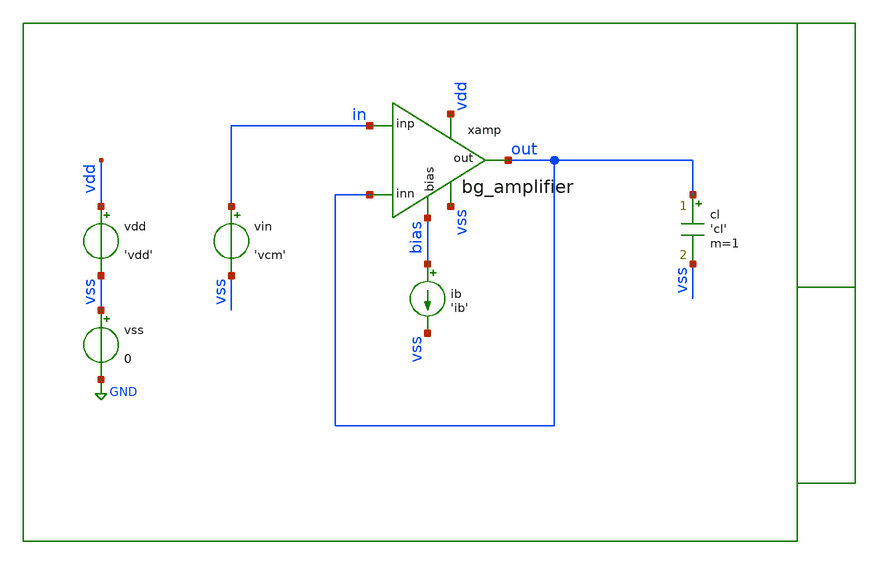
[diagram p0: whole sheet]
** sch_path: xschem/tb/bandgap_cm/bg_amplifier/dc_bg_amplifier_icmr.sch
**.subckt dc_bg_amplifier_icmr
vin in vss 'vcm'
vdd vdd vss 'vdd'
vss vss GND 0
cl out vss 'cl' m=1
xamp vdd out in out vss bias bg_amplifier
ib bias vss 'ib'
**** begin user architecture code
 *Control

.param vdd=3.3
.param vcm='vdd/2'
.param ib=1u
.param cl=1p

.csparam ctrlvdd = 'vdd'

.control
save all

* vout/vin = Avol/(1+Avol*Beta)

let gain_threshold = 60
let avol = 10^(gain_threshold/20)
let threshold = avol/(1+avol)

let vstart = 0.3
let vend   = 1.0
dc vin $&vstart $&vend 0.01
let ratio = v(out)/v(in)
meas dc vin_min when ratio=threshold rise=1
let icmr_min = vin_min
print vin_min
print icmr_min

let vstart = $&ctrlvdd - 1.0
let vend   = $&ctrlvdd
dc vin $&vstart $&vend 0.01
let ratio = v(out)/v(in)
meas dc vin_max when ratio=threshold fall=1
print vin_max
let icmr_max = $&ctrlvdd - vin_max
print icmr_max

setplot dc1
gnuplot p1 ratio
setplot dc2
gnuplot p2 ratio

.endc

 * Model Corners

.include $::CORNERS/ngspice/tt.spice
*.include $::CORNERS/ngspice/ff.spice
*.include $::CORNERS/ngspice/ss.spice
*.include $::CORNERS/ngspice/sf.spice
*.include $::CORNERS/ngspice/fs.spice

 * extract

* pex
*.include $::DESIGN_PATH/sch/bandgap_cm/bg_amplifier/bg_amplifier.pex.spice

**** end user architecture code
**.ends

* expanding   symbol:  sch/bandgap_cm/bg_amplifier/bg_amplifier.sym # of pins=6
** sym_path: xschem/sch/bandgap_cm/bg_amplifier/bg_amplifier.sym
** sch_path: xschem/sch/bandgap_cm/bg_amplifier/bg_amplifier.sch
.subckt bg_amplifier vdd out inp inn vss bias
*.ipin inn
*.ipin inp
*.opin out
*.iopin bias
*.iopin vdd
*.iopin vss
XMB5 vbn1 vbn1 vss vss nfet_06v0 L=2u W=16u nf=2 ad='int((nf+1)/2) * W/nf * 0.18u' as='int((nf+2)/2) * W/nf * 0.18u'
+ pd='2*int((nf+1)/2) * (W/nf + 0.18u)' ps='2*int((nf+2)/2) * (W/nf + 0.18u)' nrd='0.18u / W' nrs='0.18u / W'
+ sa=0 sb=0 sd=0 m=4 par=4
XMC1 von vbn1 vss vss nfet_06v0 L=2u W=16u nf=2 ad='int((nf+1)/2) * W/nf * 0.18u' as='int((nf+2)/2) * W/nf * 0.18u'
+ pd='2*int((nf+1)/2) * (W/nf + 0.18u)' ps='2*int((nf+2)/2) * (W/nf + 0.18u)' nrd='0.18u / W' nrs='0.18u / W'
+ sa=0 sb=0 sd=0 m=10 par=10
XMC2 vop vbn1 vss vss nfet_06v0 L=2u W=16u nf=2 ad='int((nf+1)/2) * W/nf * 0.18u' as='int((nf+2)/2) * W/nf * 0.18u'
+ pd='2*int((nf+1)/2) * (W/nf + 0.18u)' ps='2*int((nf+2)/2) * (W/nf + 0.18u)' nrd='0.18u / W' nrs='0.18u / W'
+ sa=0 sb=0 sd=0 m=10 par=10
XMC3 mirr vbn2 von vss nfet_06v0 L=2u W=16u nf=2 ad='int((nf+1)/2) * W/nf * 0.18u' as='int((nf+2)/2) * W/nf * 0.18u'
+ pd='2*int((nf+1)/2) * (W/nf + 0.18u)' ps='2*int((nf+2)/2) * (W/nf + 0.18u)' nrd='0.18u / W' nrs='0.18u / W'
+ sa=0 sb=0 sd=0 m=4 par=4
XMC4 out vbn2 vop vss nfet_06v0 L=2u W=16u nf=2 ad='int((nf+1)/2) * W/nf * 0.18u' as='int((nf+2)/2) * W/nf * 0.18u'
+ pd='2*int((nf+1)/2) * (W/nf + 0.18u)' ps='2*int((nf+2)/2) * (W/nf + 0.18u)' nrd='0.18u / W' nrs='0.18u / W'
+ sa=0 sb=0 sd=0 m=4 par=4
XMB3 bias bias vbp1 vdd pfet_06v0 L=2u W=16u nf=2 ad='int((nf+1)/2) * W/nf * 0.18u' as='int((nf+2)/2) * W/nf * 0.18u'
+ pd='2*int((nf+1)/2) * (W/nf + 0.18u)' ps='2*int((nf+2)/2) * (W/nf + 0.18u)' nrd='0.18u / W' nrs='0.18u / W'
+ sa=0 sb=0 sd=0 m=2 par=2
XMB1 vbp1 vbp1 vdd vdd pfet_06v0 L=2u W=16u nf=2 ad='int((nf+1)/2) * W/nf * 0.18u' as='int((nf+2)/2) * W/nf * 0.18u'
+ pd='2*int((nf+1)/2) * (W/nf + 0.18u)' ps='2*int((nf+2)/2) * (W/nf + 0.18u)' nrd='0.18u / W' nrs='0.18u / W'
+ sa=0 sb=0 sd=0 m=4 par=4
XMB2 vbn2 vbp1 vdd vdd pfet_06v0 L=2u W=16u nf=2 ad='int((nf+1)/2) * W/nf * 0.18u' as='int((nf+2)/2) * W/nf * 0.18u'
+ pd='2*int((nf+1)/2) * (W/nf + 0.18u)' ps='2*int((nf+2)/2) * (W/nf + 0.18u)' nrd='0.18u / W' nrs='0.18u / W'
+ sa=0 sb=0 sd=0 m=4 par=4
XMT1 vcm vbp1 vdd vdd pfet_06v0 L=2u W=16u nf=2 ad='int((nf+1)/2) * W/nf * 0.18u' as='int((nf+2)/2) * W/nf * 0.18u'
+ pd='2*int((nf+1)/2) * (W/nf + 0.18u)' ps='2*int((nf+2)/2) * (W/nf + 0.18u)' nrd='0.18u / W' nrs='0.18u / W'
+ sa=0 sb=0 sd=0 m=8 par=8
XMD1 von inp vcm vdd pfet_06v0 L=4u W=16u nf=2 ad='int((nf+1)/2) * W/nf * 0.18u' as='int((nf+2)/2) * W/nf * 0.18u'
+ pd='2*int((nf+1)/2) * (W/nf + 0.18u)' ps='2*int((nf+2)/2) * (W/nf + 0.18u)' nrd='0.18u / W' nrs='0.18u / W'
+ sa=0 sb=0 sd=0 m=4 par=4
XMD2 vop inn vcm vdd pfet_06v0 L=4u W=16u nf=2 ad='int((nf+1)/2) * W/nf * 0.18u' as='int((nf+2)/2) * W/nf * 0.18u'
+ pd='2*int((nf+1)/2) * (W/nf + 0.18u)' ps='2*int((nf+2)/2) * (W/nf + 0.18u)' nrd='0.18u / W' nrs='0.18u / W'
+ sa=0 sb=0 sd=0 m=4 par=4
XMC7 vda mirr vdd vdd pfet_06v0 L=2u W=16u nf=2 ad='int((nf+1)/2) * W/nf * 0.18u' as='int((nf+2)/2) * W/nf * 0.18u'
+ pd='2*int((nf+1)/2) * (W/nf + 0.18u)' ps='2*int((nf+2)/2) * (W/nf + 0.18u)' nrd='0.18u / W' nrs='0.18u / W'
+ sa=0 sb=0 sd=0 m=2 par=2
XMC8 vdb mirr vdd vdd pfet_06v0 L=2u W=16u nf=2 ad='int((nf+1)/2) * W/nf * 0.18u' as='int((nf+2)/2) * W/nf * 0.18u'
+ pd='2*int((nf+1)/2) * (W/nf + 0.18u)' ps='2*int((nf+2)/2) * (W/nf + 0.18u)' nrd='0.18u / W' nrs='0.18u / W'
+ sa=0 sb=0 sd=0 m=2 par=2
XMC5 mirr bias vda vdd pfet_06v0 L=2u W=16u nf=2 ad='int((nf+1)/2) * W/nf * 0.18u' as='int((nf+2)/2) * W/nf * 0.18u'
+ pd='2*int((nf+1)/2) * (W/nf + 0.18u)' ps='2*int((nf+2)/2) * (W/nf + 0.18u)' nrd='0.18u / W' nrs='0.18u / W'
+ sa=0 sb=0 sd=0 m=4 par=4
XMC6 out bias vdb vdd pfet_06v0 L=2u W=16u nf=2 ad='int((nf+1)/2) * W/nf * 0.18u' as='int((nf+2)/2) * W/nf * 0.18u'
+ pd='2*int((nf+1)/2) * (W/nf + 0.18u)' ps='2*int((nf+2)/2) * (W/nf + 0.18u)' nrd='0.18u / W' nrs='0.18u / W'
+ sa=0 sb=0 sd=0 m=4 par=4
XMB4 vbn2 vbn2 vbn1 vss nfet_06v0 L=2u W=16u nf=2 ad='int((nf+1)/2) * W/nf * 0.18u' as='int((nf+2)/2) * W/nf * 0.18u'
+ pd='2*int((nf+1)/2) * (W/nf + 0.18u)' ps='2*int((nf+2)/2) * (W/nf + 0.18u)' nrd='0.18u / W' nrs='0.18u / W'
+ sa=0 sb=0 sd=0 m=4 par=4
XMDUM1 vdd vdd vdd vdd pfet_06v0 L=2u W=16u nf=2 ad='int((nf+1)/2) * W/nf * 0.18u' as='int((nf+2)/2) * W/nf * 0.18u'
+ pd='2*int((nf+1)/2) * (W/nf + 0.18u)' ps='2*int((nf+2)/2) * (W/nf + 0.18u)' nrd='0.18u / W' nrs='0.18u / W'
+ sa=0 sb=0 sd=0 m=4 par=4
XMDUM2 vdd vdd vdd vdd pfet_06v0 L=2u W=16u nf=2 ad='int((nf+1)/2) * W/nf * 0.18u' as='int((nf+2)/2) * W/nf * 0.18u'
+ pd='2*int((nf+1)/2) * (W/nf + 0.18u)' ps='2*int((nf+2)/2) * (W/nf + 0.18u)' nrd='0.18u / W' nrs='0.18u / W'
+ sa=0 sb=0 sd=0 m=4 par=4
XMDUM3 vdd vdd vdd vdd pfet_06v0 L=2u W=16u nf=2 ad='int((nf+1)/2) * W/nf * 0.18u' as='int((nf+2)/2) * W/nf * 0.18u'
+ pd='2*int((nf+1)/2) * (W/nf + 0.18u)' ps='2*int((nf+2)/2) * (W/nf + 0.18u)' nrd='0.18u / W' nrs='0.18u / W'
+ sa=0 sb=0 sd=0 m=2 par=2
XMDUM4 vss vss vss vss nfet_06v0 L=2u W=16u nf=2 ad='int((nf+1)/2) * W/nf * 0.18u' as='int((nf+2)/2) * W/nf * 0.18u'
+ pd='2*int((nf+1)/2) * (W/nf + 0.18u)' ps='2*int((nf+2)/2) * (W/nf + 0.18u)' nrd='0.18u / W' nrs='0.18u / W'
+ sa=0 sb=0 sd=0 m=2 par=2
XMDUM5 vss vss vss vss nfet_06v0 L=2u W=16u nf=2 ad='int((nf+1)/2) * W/nf * 0.18u' as='int((nf+2)/2) * W/nf * 0.18u'
+ pd='2*int((nf+1)/2) * (W/nf + 0.18u)' ps='2*int((nf+2)/2) * (W/nf + 0.18u)' nrd='0.18u / W' nrs='0.18u / W'
+ sa=0 sb=0 sd=0 m=2 par=2
XMDUM6 vdd vdd vdd vdd pfet_06v0 L=4u W=16u nf=2 ad='int((nf+1)/2) * W/nf * 0.18u' as='int((nf+2)/2) * W/nf * 0.18u'
+ pd='2*int((nf+1)/2) * (W/nf + 0.18u)' ps='2*int((nf+2)/2) * (W/nf + 0.18u)' nrd='0.18u / W' nrs='0.18u / W'
+ sa=0 sb=0 sd=0 m=16 par=16
.ends

.GLOBAL GND
.end
